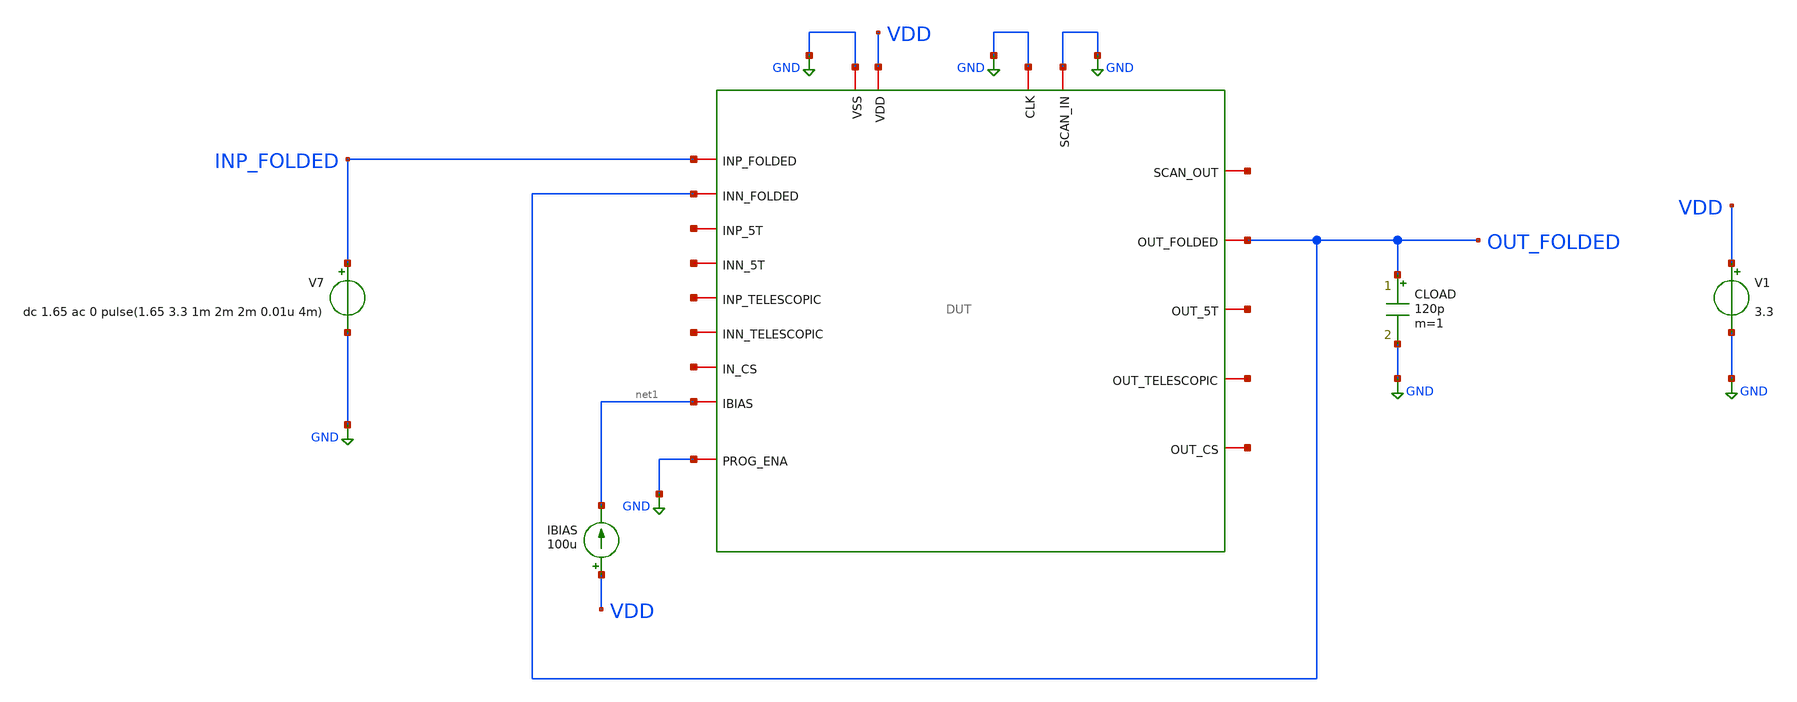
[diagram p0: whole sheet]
** sch_path: designs/libs/verification/ota_folded/default_sizing/large_signal_upper_swing_tb.sch
**.subckt large_signal_upper_swing_tb
x1 GND net2 GND GND VDD OUT_FOLDED INP_FOLDED net3 net1 OUT_FOLDED net4 net5 net6 net7 net8 net9
+ net10 GND DUT
V1 VDD GND 3.3
CLOAD OUT_FOLDED GND 120p m=1
V7 INP_FOLDED GND dc 1.65 ac 0 pulse(1.65 3.3 1m 2m 2m 0.01u 4m)
IBIAS VDD net1 100u
**** begin user architecture code

.include $::180MCU_MODELS/design.ngspice
.lib $::180MCU_MODELS/sm141064.ngspice typical



.control
tran 1u 5m

plot v(out_folded) v(inp_folded)

let error = v(out_folded) - v(inp_folded)
plot error

meas tran t_clip when error = -0.019 cross = 1
print t_clip

meas tran vout_clip find v(out_folded) at = t_clip
meas tran vin_clip find v(inp_folded) at = t_clip
print vout_clip vin_clip
.endc


**** end user architecture code
**.ends
.GLOBAL GND
.end
